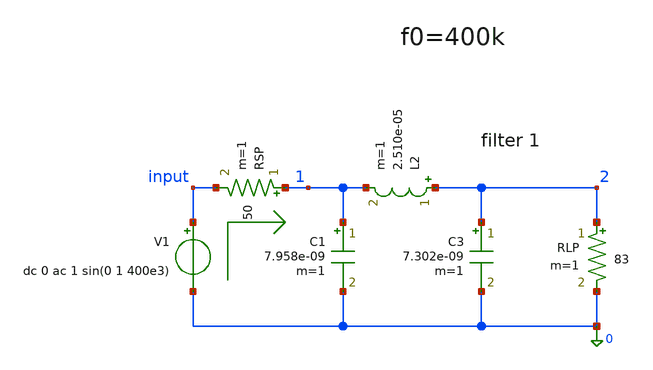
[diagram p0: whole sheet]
** sch_path: circuitos/exemplo05.sch
**.subckt exemplo05
C1 1 0 7.958e-09 m=1
V1 input 0 dc 0 ac 1 sin(0 1 400e3)
RLP 2 0 83 m=1
RSP 1 input 50 m=1
L2 2 1 2.510e-05 m=1
C3 2 0 7.302e-09 m=1
**** begin user architecture code

.control
op
ac dec 101 1e2 1e6
tran 1ns 0.2ms

setplot ac1

plot xlog real(v(1)/-v1#branch)
plot xlog imag(v(1)/-v1#branch)

setplot tran1
plot v(2)
.endc

**** end user architecture code
**.ends
.end
